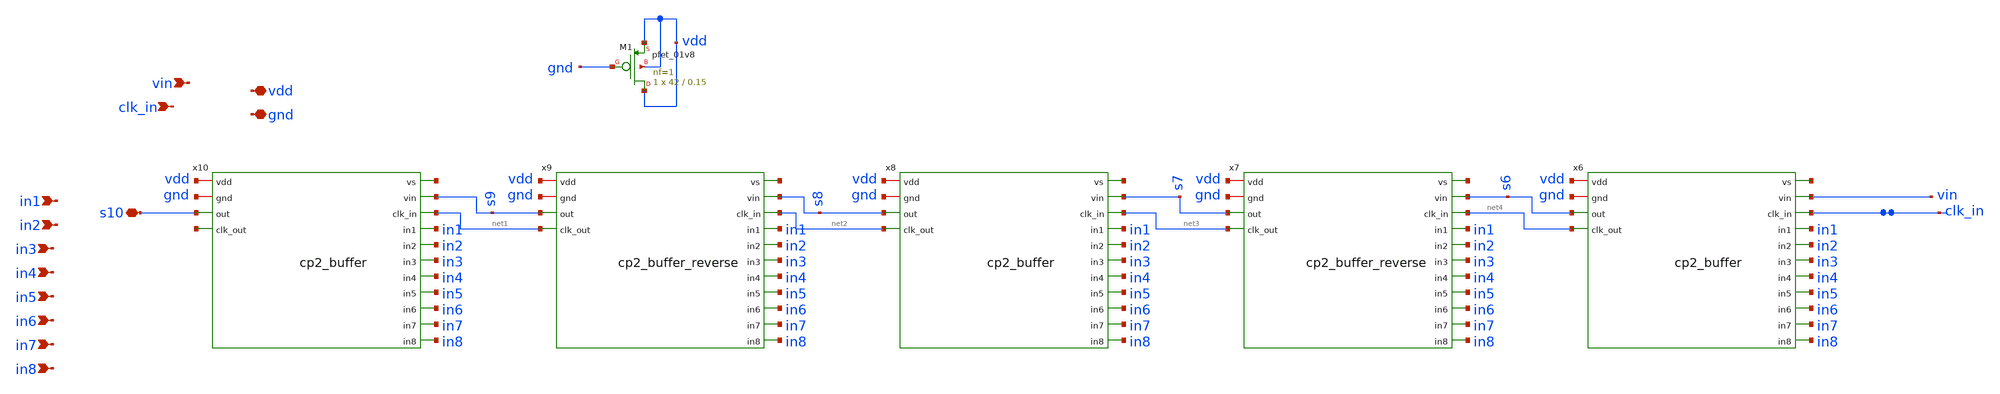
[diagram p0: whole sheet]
** sch_path: xschem/NK_CP2_5stage.sch
**.subckt NK_CP2_5stage in1 in2 in3 in4 in5 in6 in7 in8 gnd vdd vin clk_in s10
*.ipin in1
*.ipin in2
*.ipin in3
*.ipin in4
*.ipin in5
*.ipin in6
*.ipin in7
*.ipin in8
*.iopin gnd
*.iopin vdd
*.ipin vin
*.ipin clk_in
*.iopin s10
x6 net5 vin vdd clk_in gnd in1 s6 in2 in3 in4 in5 in6 in7 in8 net4 cp2_buffer
x7 net6 s6 vdd net4 gnd in1 s7 in2 in3 in4 in5 in6 in7 in8 net3 cp2_buffer_reverse
x8 net7 s7 vdd net3 gnd in1 s8 in2 in3 in4 in5 in6 in7 in8 net2 cp2_buffer
x9 net8 s8 vdd net2 gnd in1 s9 in2 in3 in4 in5 in6 in7 in8 net1 cp2_buffer_reverse
x10 net9 s9 vdd net1 gnd in1 s10 in2 in3 in4 in5 in6 in7 in8 net10 cp2_buffer
XM1 vdd gnd vdd vdd sky130_fd_pr__pfet_01v8 L=0.15 W=42 nf=1 ad='int((nf+1)/2) * W/nf * 0.29' as='int((nf+2)/2) * W/nf * 0.29'
+ pd='2*int((nf+1)/2) * (W/nf + 0.29)' ps='2*int((nf+2)/2) * (W/nf + 0.29)' nrd='0.29 / W' nrs='0.29 / W'
+ sa=0 sb=0 sd=0 mult=1 m=1
**.ends
.end
